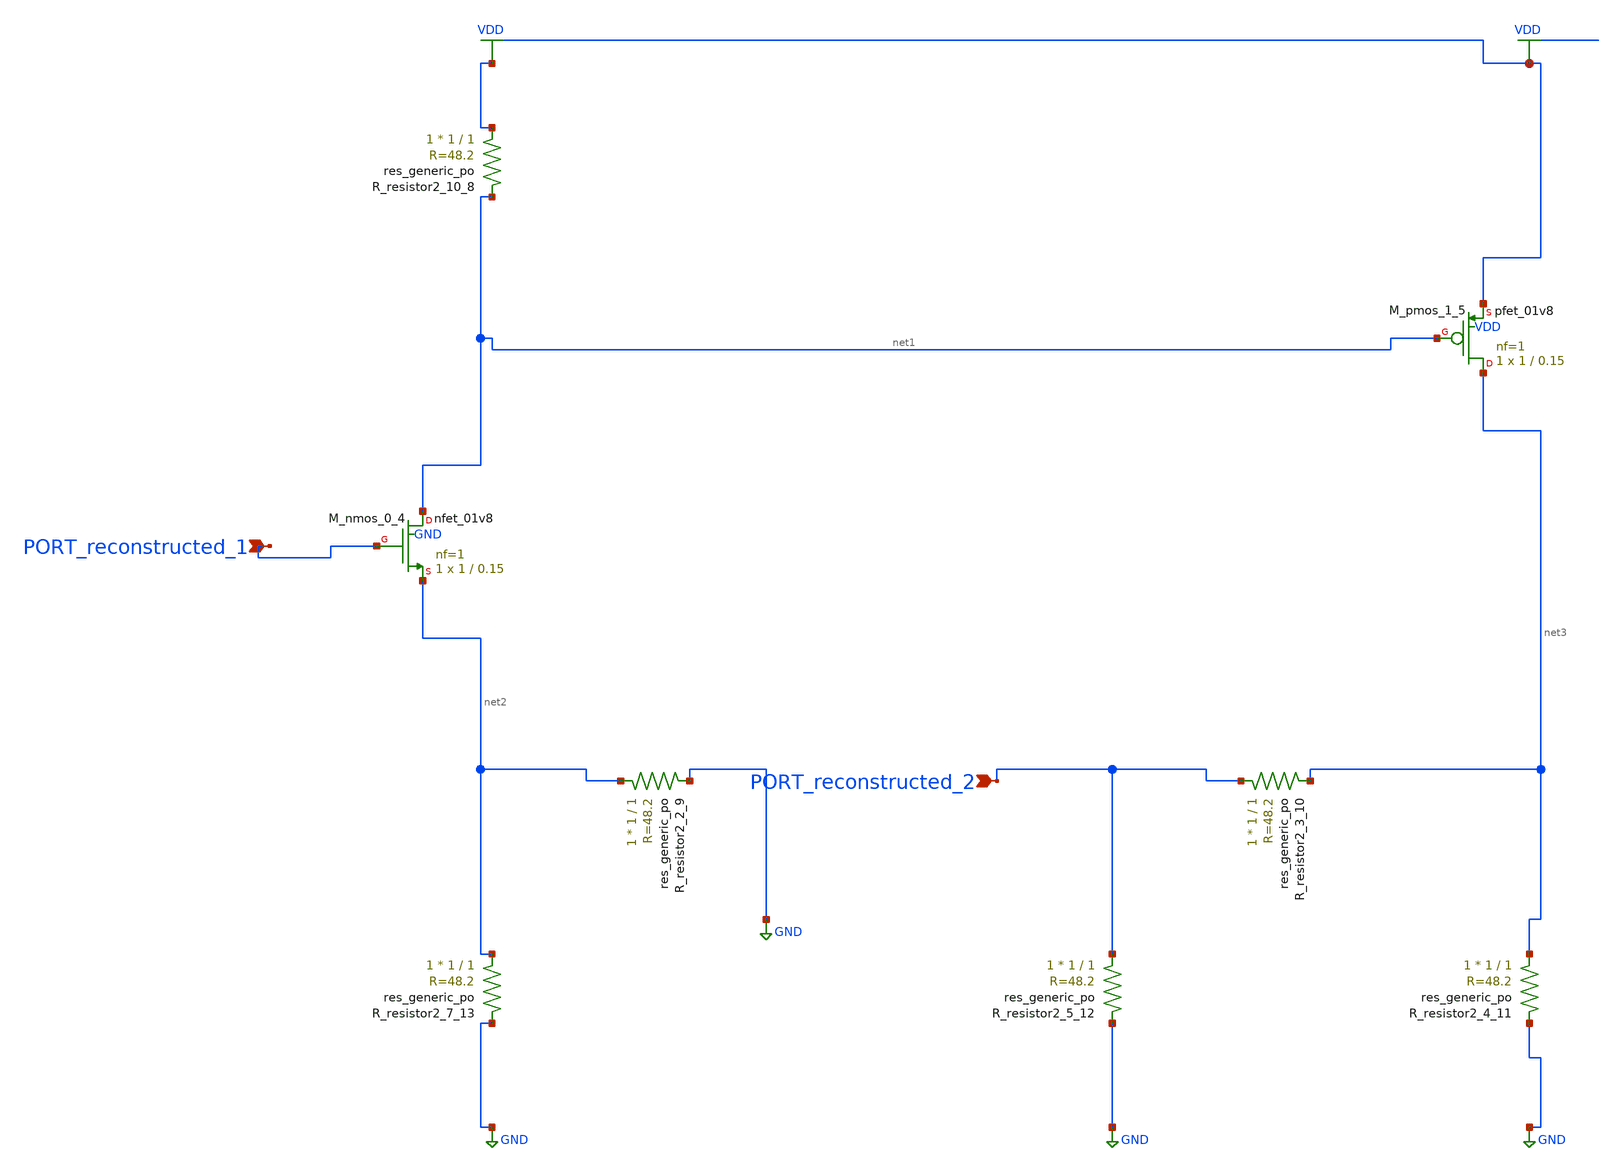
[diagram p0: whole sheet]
** sch_path: schematics/AMSNet/577.sch
**.subckt 577 PORT_reconstructed_1 PORT_reconstructed_2
*.ipin PORT_reconstructed_1
*.ipin PORT_reconstructed_2
XM_nmos_0_4 net1 PORT_reconstructed_1 net2 GND sky130_fd_pr__nfet_01v8 L=0.15 W=1 nf=1 ad='int((1 + 1)/2) * 1 / 1 * 0.29'
+ as='int((1 + 2)/2) * 1 / 1 * 0.29' pd='2*int((1 + 1)/2) * (1 / 1 + 0.29)' ps='2*int((1 + 2)/2) * (1 / 1 + 0.29)'
+ nrd='0.29 / 1 ' nrs='0.29 / 1 ' sa=0 sb=0 sd=0 mult=1 m=1
XM_pmos_1_5 net3 net1 VDD VDD sky130_fd_pr__pfet_01v8 L=0.15 W=1 nf=1 ad='int((1 + 1)/2) * 1 / 1 * 0.29'
+ as='int((1 + 2)/2) * 1 / 1 * 0.29' pd='2*int((1 + 1)/2) * (1 / 1 + 0.29)' ps='2*int((1 + 2)/2) * (1 / 1 + 0.29)'
+ nrd='0.29 / 1 ' nrs='0.29 / 1 ' sa=0 sb=0 sd=0 mult=1 m=1
XR_resistor2_10_8 VDD net1 sky130_fd_pr__res_generic_po W=1 L=1 m=1
XR_resistor2_2_9 net2 GND sky130_fd_pr__res_generic_po W=1 L=1 m=1
XR_resistor2_3_10 PORT_reconstructed_2 net3 sky130_fd_pr__res_generic_po W=1 L=1 m=1
XR_resistor2_4_11 net3 GND sky130_fd_pr__res_generic_po W=1 L=1 m=1
XR_resistor2_5_12 PORT_reconstructed_2 GND sky130_fd_pr__res_generic_po W=1 L=1 m=1
XR_resistor2_7_13 net2 GND sky130_fd_pr__res_generic_po W=1 L=1 m=1
**.ends
.GLOBAL GND
.GLOBAL VDD
.end
